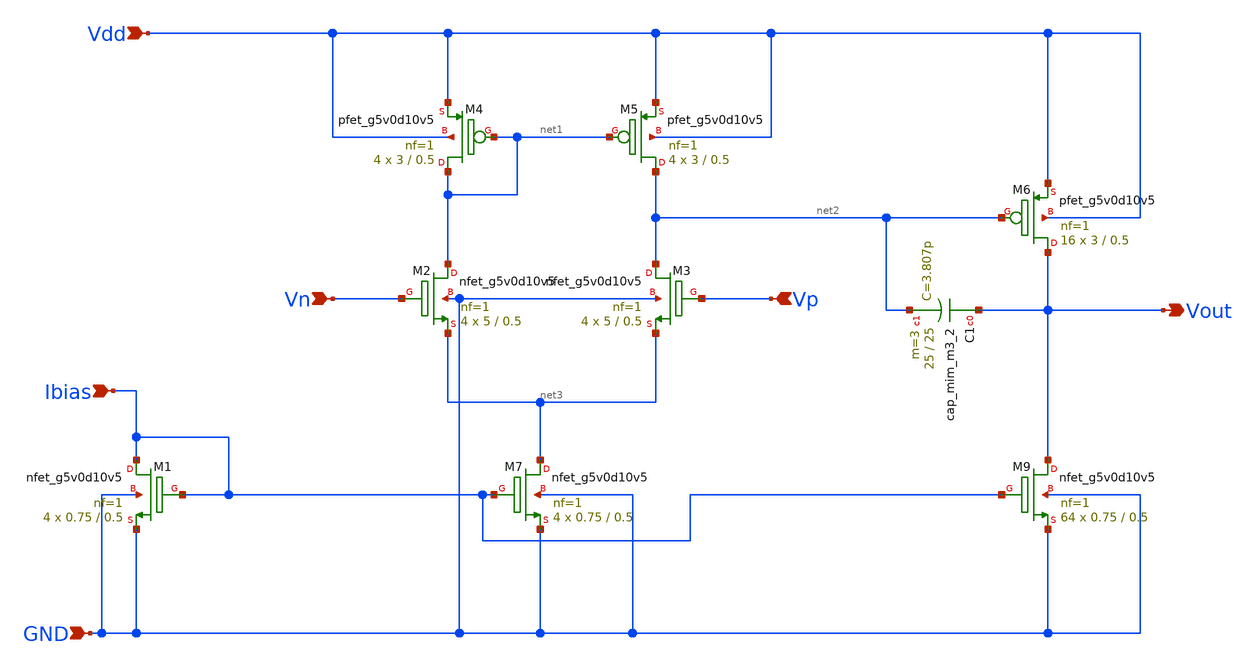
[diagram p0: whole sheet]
** sch_path: Analog_Blocks/LDO/Schematic/LDO_Miller_1.8v/Error_Amplifier.sch
**.subckt Error_Amplifier Vout Vdd GND Vp Vn Ibias
*.opin Vout
*.ipin Vdd
*.ipin GND
*.ipin Vp
*.ipin Vn
*.ipin Ibias
XM2 net1 Vn net3 GND sky130_fd_pr__nfet_g5v0d10v5 L=0.5 W=5 nf=1 ad='int((nf+1)/2) * W/nf * 0.29' as='int((nf+2)/2) * W/nf * 0.29'
+ pd='2*int((nf+1)/2) * (W/nf + 0.29)' ps='2*int((nf+2)/2) * (W/nf + 0.29)' nrd='0.29 / W' nrs='0.29 / W'
+ sa=0 sb=0 sd=0 mult=4 m=4
XM3 net2 Vp net3 GND sky130_fd_pr__nfet_g5v0d10v5 L=0.5 W=5 nf=1 ad='int((nf+1)/2) * W/nf * 0.29' as='int((nf+2)/2) * W/nf * 0.29'
+ pd='2*int((nf+1)/2) * (W/nf + 0.29)' ps='2*int((nf+2)/2) * (W/nf + 0.29)' nrd='0.29 / W' nrs='0.29 / W'
+ sa=0 sb=0 sd=0 mult=4 m=4
XM4 net1 net1 Vdd Vdd sky130_fd_pr__pfet_g5v0d10v5 L=0.5 W=3 nf=1 ad='int((nf+1)/2) * W/nf * 0.29' as='int((nf+2)/2) * W/nf * 0.29'
+ pd='2*int((nf+1)/2) * (W/nf + 0.29)' ps='2*int((nf+2)/2) * (W/nf + 0.29)' nrd='0.29 / W' nrs='0.29 / W'
+ sa=0 sb=0 sd=0 mult=4 m=4
XM5 net2 net1 Vdd Vdd sky130_fd_pr__pfet_g5v0d10v5 L=0.5 W=3 nf=1 ad='int((nf+1)/2) * W/nf * 0.29' as='int((nf+2)/2) * W/nf * 0.29'
+ pd='2*int((nf+1)/2) * (W/nf + 0.29)' ps='2*int((nf+2)/2) * (W/nf + 0.29)' nrd='0.29 / W' nrs='0.29 / W'
+ sa=0 sb=0 sd=0 mult=4 m=4
XM6 Vout net2 Vdd Vdd sky130_fd_pr__pfet_g5v0d10v5 L=0.5 W=3 nf=1 ad='int((nf+1)/2) * W/nf * 0.29' as='int((nf+2)/2) * W/nf * 0.29'
+ pd='2*int((nf+1)/2) * (W/nf + 0.29)' ps='2*int((nf+2)/2) * (W/nf + 0.29)' nrd='0.29 / W' nrs='0.29 / W'
+ sa=0 sb=0 sd=0 mult=16 m=16
XM7 net3 Ibias GND GND sky130_fd_pr__nfet_g5v0d10v5 L=0.5 W=0.75 nf=1 ad='int((nf+1)/2) * W/nf * 0.29'
+ as='int((nf+2)/2) * W/nf * 0.29' pd='2*int((nf+1)/2) * (W/nf + 0.29)' ps='2*int((nf+2)/2) * (W/nf + 0.29)'
+ nrd='0.29 / W' nrs='0.29 / W' sa=0 sb=0 sd=0 mult=4 m=4
XM9 Vout Ibias GND GND sky130_fd_pr__nfet_g5v0d10v5 L=0.5 W=0.75 nf=1 ad='int((nf+1)/2) * W/nf * 0.29'
+ as='int((nf+2)/2) * W/nf * 0.29' pd='2*int((nf+1)/2) * (W/nf + 0.29)' ps='2*int((nf+2)/2) * (W/nf + 0.29)'
+ nrd='0.29 / W' nrs='0.29 / W' sa=0 sb=0 sd=0 mult=64 m=64
XM1 Ibias Ibias GND GND sky130_fd_pr__nfet_g5v0d10v5 L=0.5 W=0.75 nf=1 ad='int((nf+1)/2) * W/nf * 0.29'
+ as='int((nf+2)/2) * W/nf * 0.29' pd='2*int((nf+1)/2) * (W/nf + 0.29)' ps='2*int((nf+2)/2) * (W/nf + 0.29)'
+ nrd='0.29 / W' nrs='0.29 / W' sa=0 sb=0 sd=0 mult=4 m=4
XC1 Vout net2 sky130_fd_pr__cap_mim_m3_2 W=25 L=25 MF=3 m=3
**.ends
.end
